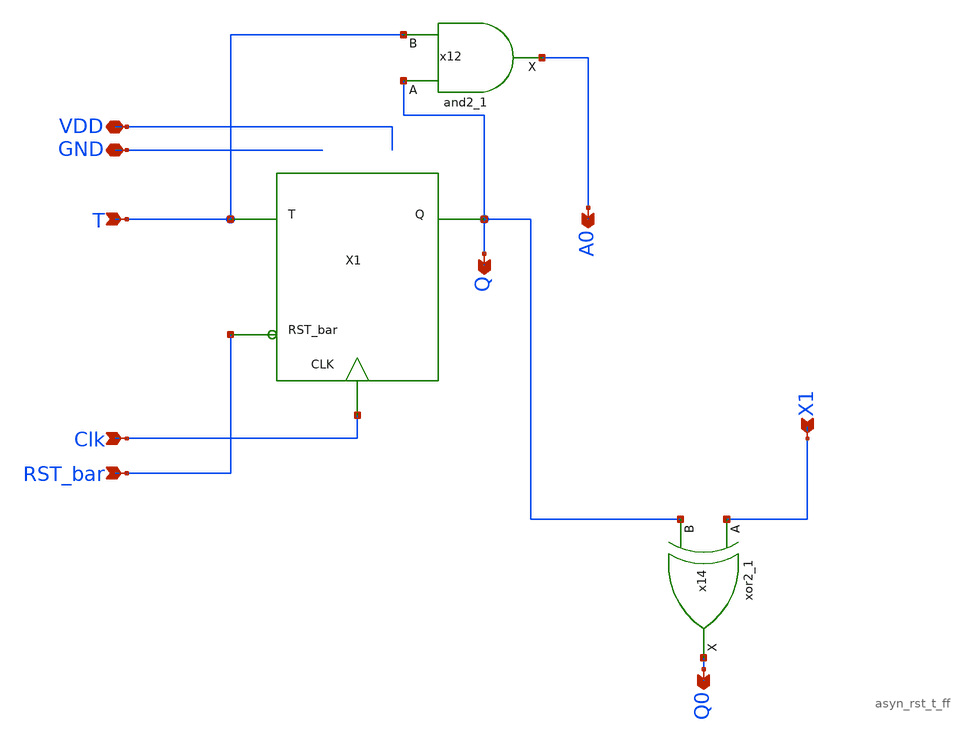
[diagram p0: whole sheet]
** sch_path: xschem/Asyn_rst_gray_counter/counter_cell.sch
**.subckt counter_cell Clk T Q0 RST_bar A0 X1 Q VDD GND
*.ipin Clk
*.ipin T
*.opin Q0
*.ipin RST_bar
*.opin A0
*.ipin X1
*.opin Q
*.iopin VDD
*.iopin GND
x14 X1 Q GND GND VDD VDD Q0 sky130_fd_sc_lp__xor2_1
x12 Q T GND GND VDD VDD A0 sky130_fd_sc_lp__and2_1
X1 T Q Clk RST_bar asyn_rst_t_ff
**.ends

* expanding   symbol:  T_flip_flop/asyn_rst_t_ff.sym # of pins=4
** sym_path: xschem/T_flip_flop/asyn_rst_t_ff.sym
** sch_path: xschem/T_flip_flop/asyn_rst_t_ff.sch
.subckt asyn_rst_t_ff T Q CLK RST_bar
*.ipin T
*.ipin CLK
*.opin Q
*.ipin RST_bar
x1 CLK net1 RST_bar GND GND VDD VDD Q sky130_fd_sc_lp__dfrtp_1
x3 T Q GND GND VDD VDD net1 sky130_fd_sc_lp__xor2_1
.ends

.end
